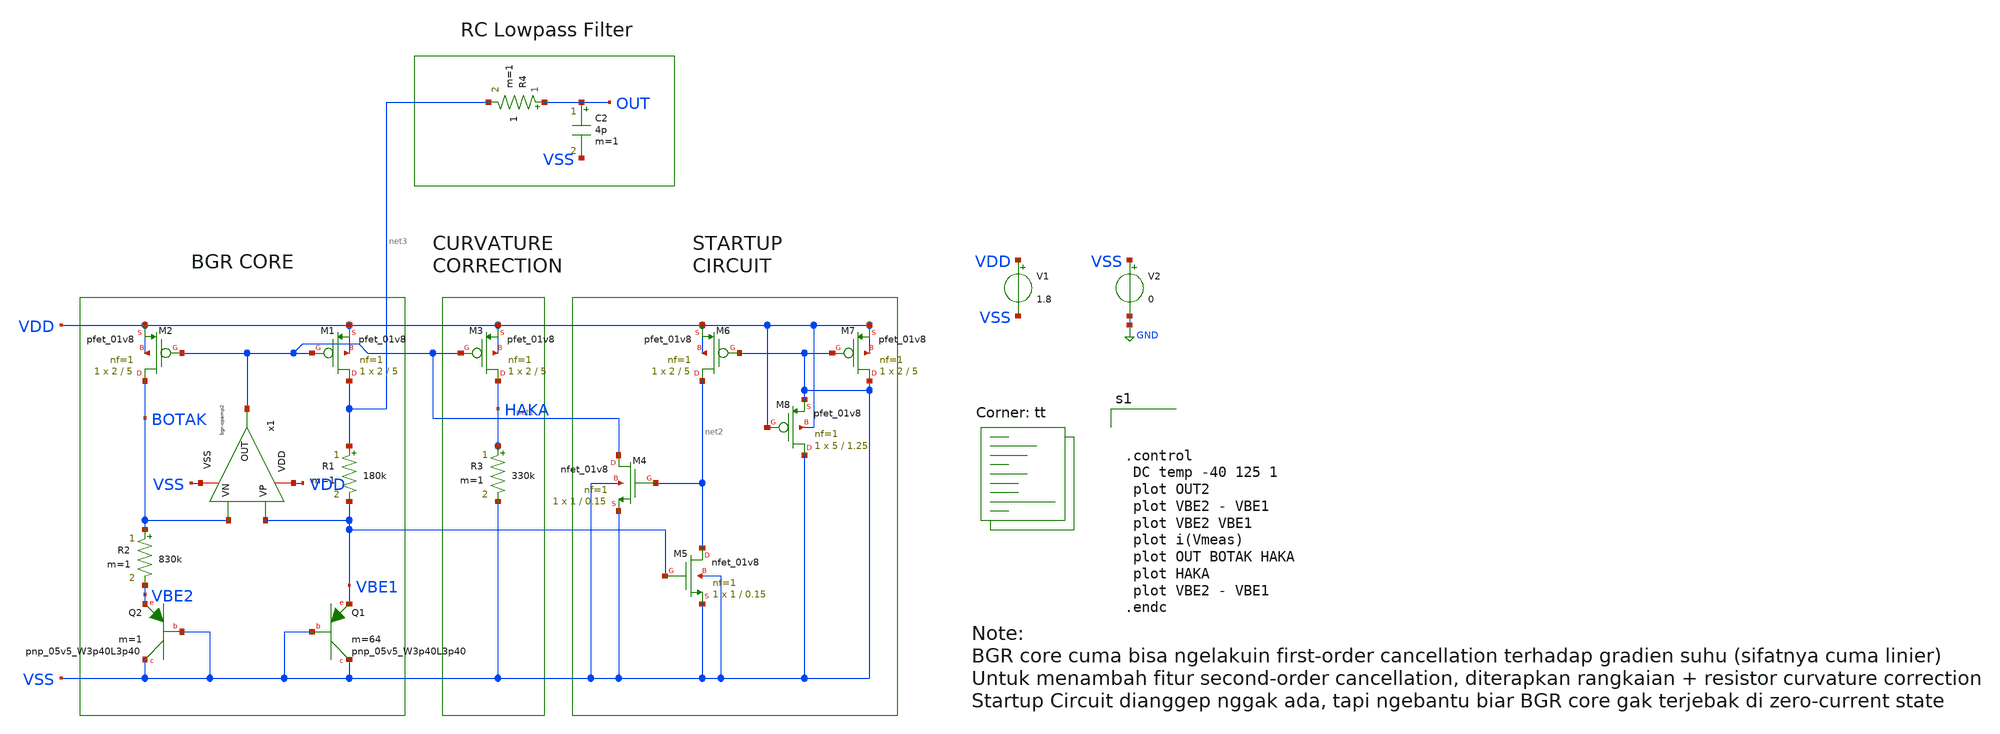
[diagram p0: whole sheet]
** sch_path: bandgap/bgr/bgr-core.sch
**.subckt bgr-core
XM1 net3 net1 VDD VDD sky130_fd_pr__pfet_01v8 L=5 W=2 nf=1 ad='int((nf+1)/2) * W/nf * 0.29' as='int((nf+2)/2) * W/nf * 0.29'
+ pd='2*int((nf+1)/2) * (W/nf + 0.29)' ps='2*int((nf+2)/2) * (W/nf + 0.29)' nrd='0.29 / W' nrs='0.29 / W'
+ sa=0 sb=0 sd=0 mult=1 m=1
XM2 BOTAK net1 VDD VDD sky130_fd_pr__pfet_01v8 L=5 W=2 nf=1 ad='int((nf+1)/2) * W/nf * 0.29' as='int((nf+2)/2) * W/nf * 0.29'
+ pd='2*int((nf+1)/2) * (W/nf + 0.29)' ps='2*int((nf+2)/2) * (W/nf + 0.29)' nrd='0.29 / W' nrs='0.29 / W'
+ sa=0 sb=0 sd=0 mult=1 m=1
R1 net3 VBE1 180k m=1
R2 BOTAK VBE2 830k m=1
XQ1 VSS VSS VBE1 sky130_fd_pr__pnp_05v5_W3p40L3p40 m=64
XQ2 VSS VSS VBE2 sky130_fd_pr__pnp_05v5_W3p40L3p40 m=1
V1 VDD VSS 1.8
V2 VSS GND 0
XM3 HAKA net1 VDD VDD sky130_fd_pr__pfet_01v8 L=5 W=2 nf=1 ad='int((nf+1)/2) * W/nf * 0.29' as='int((nf+2)/2) * W/nf * 0.29'
+ pd='2*int((nf+1)/2) * (W/nf + 0.29)' ps='2*int((nf+2)/2) * (W/nf + 0.29)' nrd='0.29 / W' nrs='0.29 / W'
+ sa=0 sb=0 sd=0 mult=1 m=1
R3 HAKA VSS 330k m=1
XM4 net1 net2 VSS VSS sky130_fd_pr__nfet_01v8 L=0.15 W=1 nf=1 ad='int((nf+1)/2) * W/nf * 0.29' as='int((nf+2)/2) * W/nf * 0.29'
+ pd='2*int((nf+1)/2) * (W/nf + 0.29)' ps='2*int((nf+2)/2) * (W/nf + 0.29)' nrd='0.29 / W' nrs='0.29 / W'
+ sa=0 sb=0 sd=0 mult=1 m=1
XM5 net2 VBE1 VSS VSS sky130_fd_pr__nfet_01v8 L=0.15 W=1 nf=1 ad='int((nf+1)/2) * W/nf * 0.29' as='int((nf+2)/2) * W/nf * 0.29'
+ pd='2*int((nf+1)/2) * (W/nf + 0.29)' ps='2*int((nf+2)/2) * (W/nf + 0.29)' nrd='0.29 / W' nrs='0.29 / W'
+ sa=0 sb=0 sd=0 mult=1 m=1
XM6 net2 VSS VDD VDD sky130_fd_pr__pfet_01v8 L=5 W=2 nf=1 ad='int((nf+1)/2) * W/nf * 0.29' as='int((nf+2)/2) * W/nf * 0.29'
+ pd='2*int((nf+1)/2) * (W/nf + 0.29)' ps='2*int((nf+2)/2) * (W/nf + 0.29)' nrd='0.29 / W' nrs='0.29 / W'
+ sa=0 sb=0 sd=0 mult=1 m=1
XM7 VSS VSS VDD VDD sky130_fd_pr__pfet_01v8 L=5 W=2 nf=1 ad='int((nf+1)/2) * W/nf * 0.29' as='int((nf+2)/2) * W/nf * 0.29'
+ pd='2*int((nf+1)/2) * (W/nf + 0.29)' ps='2*int((nf+2)/2) * (W/nf + 0.29)' nrd='0.29 / W' nrs='0.29 / W'
+ sa=0 sb=0 sd=0 mult=1 m=1
XM8 VSS VDD VSS VDD sky130_fd_pr__pfet_01v8 L=1.25 W=5 nf=1 ad='int((nf+1)/2) * W/nf * 0.29' as='int((nf+2)/2) * W/nf * 0.29'
+ pd='2*int((nf+1)/2) * (W/nf + 0.29)' ps='2*int((nf+2)/2) * (W/nf + 0.29)' nrd='0.29 / W' nrs='0.29 / W'
+ sa=0 sb=0 sd=0 mult=1 m=1
C2 OUT VSS 4p m=1
R4 OUT net3 1 m=1
x1 VDD net1 VBE1 BOTAK VSS bgr-opamp2
**** begin user architecture code
.lib $::SKYWATER_MODELS/sky130.lib.spice tt



.control
 DC temp -40 125 1
 plot OUT2
 plot VBE2 - VBE1
 plot VBE2 VBE1
 plot i(Vmeas)
 plot OUT BOTAK HAKA
 plot HAKA
 plot VBE2 - VBE1
.endc


**** end user architecture code
**.ends

* expanding   symbol:  afe-icdec-teknofest-2026/bandgap/bgr/bgr-opamp2.sym # of pins=5
** sym_path: bandgap/bgr/bgr-opamp2.sym
** sch_path: bandgap/bgr/bgr-opamp2.sch
.subckt bgr-opamp2 VDD OUT VP VN VSS
*.iopin VSS
*.iopin VDD
*.ipin VP
*.ipin VN
*.opin OUT
XR10 VSS net5 VSS sky130_fd_pr__res_high_po_1p41 L=9.235 mult=1 m=1
XM19 net2 net2 VSS VSS sky130_fd_pr__nfet_01v8_lvt L=0.5 W=6.4 nf=1 ad='int((nf+1)/2) * W/nf * 0.29'
+ as='int((nf+2)/2) * W/nf * 0.29' pd='2*int((nf+1)/2) * (W/nf + 0.29)' ps='2*int((nf+2)/2) * (W/nf + 0.29)'
+ nrd='0.29 / W' nrs='0.29 / W' sa=0 sb=0 sd=0 mult=1 m=1
XM20 net3 net2 net5 VSS sky130_fd_pr__nfet_01v8_lvt L=0.5 W=6.4 nf=1 ad='int((nf+1)/2) * W/nf * 0.29'
+ as='int((nf+2)/2) * W/nf * 0.29' pd='2*int((nf+1)/2) * (W/nf + 0.29)' ps='2*int((nf+2)/2) * (W/nf + 0.29)'
+ nrd='0.29 / W' nrs='0.29 / W' sa=0 sb=0 sd=0 mult=1 m=1
XM16 net4 net1 VDD VDD sky130_fd_pr__pfet_01v8_lvt L=0.5 W=20.8 nf=1 ad='int((nf+1)/2) * W/nf * 0.29'
+ as='int((nf+2)/2) * W/nf * 0.29' pd='2*int((nf+1)/2) * (W/nf + 0.29)' ps='2*int((nf+2)/2) * (W/nf + 0.29)'
+ nrd='0.29 / W' nrs='0.29 / W' sa=0 sb=0 sd=0 mult=1 m=1
XM13 net1 net1 VDD VDD sky130_fd_pr__pfet_01v8_lvt L=0.5 W=20.8 nf=1 ad='int((nf+1)/2) * W/nf * 0.29'
+ as='int((nf+2)/2) * W/nf * 0.29' pd='2*int((nf+1)/2) * (W/nf + 0.29)' ps='2*int((nf+2)/2) * (W/nf + 0.29)'
+ nrd='0.29 / W' nrs='0.29 / W' sa=0 sb=0 sd=0 mult=1 m=1
XM14 net2 net3 net4 VDD sky130_fd_pr__pfet_01v8_lvt L=0.5 W=20.8 nf=1 ad='int((nf+1)/2) * W/nf * 0.29'
+ as='int((nf+2)/2) * W/nf * 0.29' pd='2*int((nf+1)/2) * (W/nf + 0.29)' ps='2*int((nf+2)/2) * (W/nf + 0.29)'
+ nrd='0.29 / W' nrs='0.29 / W' sa=0 sb=0 sd=0 mult=1 m=1
XM17 net3 net3 net1 VDD sky130_fd_pr__pfet_01v8_lvt L=0.5 W=20.8 nf=1 ad='int((nf+1)/2) * W/nf * 0.29'
+ as='int((nf+2)/2) * W/nf * 0.29' pd='2*int((nf+1)/2) * (W/nf + 0.29)' ps='2*int((nf+2)/2) * (W/nf + 0.29)'
+ nrd='0.29 / W' nrs='0.29 / W' sa=0 sb=0 sd=0 mult=1 m=1
XM18 net6 net1 VDD VDD sky130_fd_pr__pfet_01v8_lvt L=0.5 W=20.8 nf=1 ad='int((nf+1)/2) * W/nf * 0.29'
+ as='int((nf+2)/2) * W/nf * 0.29' pd='2*int((nf+1)/2) * (W/nf + 0.29)' ps='2*int((nf+2)/2) * (W/nf + 0.29)'
+ nrd='0.29 / W' nrs='0.29 / W' sa=0 sb=0 sd=0 mult=1 m=1
XM21 net7 net3 net6 VDD sky130_fd_pr__pfet_01v8_lvt L=0.5 W=20.8 nf=1 ad='int((nf+1)/2) * W/nf * 0.29'
+ as='int((nf+2)/2) * W/nf * 0.29' pd='2*int((nf+1)/2) * (W/nf + 0.29)' ps='2*int((nf+2)/2) * (W/nf + 0.29)'
+ nrd='0.29 / W' nrs='0.29 / W' sa=0 sb=0 sd=0 mult=1 m=1
XM22 net7 net7 net9 VSS sky130_fd_pr__nfet_01v8_lvt L=0.5 W=1.45 nf=1 ad='int((nf+1)/2) * W/nf * 0.29'
+ as='int((nf+2)/2) * W/nf * 0.29' pd='2*int((nf+1)/2) * (W/nf + 0.29)' ps='2*int((nf+2)/2) * (W/nf + 0.29)'
+ nrd='0.29 / W' nrs='0.29 / W' sa=0 sb=0 sd=0 mult=1 m=1
XM23 net9 net7 net8 VSS sky130_fd_pr__nfet_01v8_lvt L=0.5 W=1.45 nf=1 ad='int((nf+1)/2) * W/nf * 0.29'
+ as='int((nf+2)/2) * W/nf * 0.29' pd='2*int((nf+1)/2) * (W/nf + 0.29)' ps='2*int((nf+2)/2) * (W/nf + 0.29)'
+ nrd='0.29 / W' nrs='0.29 / W' sa=0 sb=0 sd=0 mult=1 m=1
XM24 net8 net7 VSS VSS sky130_fd_pr__nfet_01v8_lvt L=0.5 W=1.45 nf=1 ad='int((nf+1)/2) * W/nf * 0.29'
+ as='int((nf+2)/2) * W/nf * 0.29' pd='2*int((nf+1)/2) * (W/nf + 0.29)' ps='2*int((nf+2)/2) * (W/nf + 0.29)'
+ nrd='0.29 / W' nrs='0.29 / W' sa=0 sb=0 sd=0 mult=1 m=1
XM26 net15 VN net10 VDD sky130_fd_pr__pfet_01v8_lvt L=1.25 W=30 nf=1 ad='int((nf+1)/2) * W/nf * 0.29'
+ as='int((nf+2)/2) * W/nf * 0.29' pd='2*int((nf+1)/2) * (W/nf + 0.29)' ps='2*int((nf+2)/2) * (W/nf + 0.29)'
+ nrd='0.29 / W' nrs='0.29 / W' sa=0 sb=0 sd=0 mult=1 m=1
XM27 net14 VP net10 VDD sky130_fd_pr__pfet_01v8_lvt L=1.25 W=30 nf=1 ad='int((nf+1)/2) * W/nf * 0.29'
+ as='int((nf+2)/2) * W/nf * 0.29' pd='2*int((nf+1)/2) * (W/nf + 0.29)' ps='2*int((nf+2)/2) * (W/nf + 0.29)'
+ nrd='0.29 / W' nrs='0.29 / W' sa=0 sb=0 sd=0 mult=1 m=1
XM15 net10 net1 VDD VDD sky130_fd_pr__pfet_01v8_lvt L=1.25 W=20.8 nf=1 ad='int((nf+1)/2) * W/nf * 0.29'
+ as='int((nf+2)/2) * W/nf * 0.29' pd='2*int((nf+1)/2) * (W/nf + 0.29)' ps='2*int((nf+2)/2) * (W/nf + 0.29)'
+ nrd='0.29 / W' nrs='0.29 / W' sa=0 sb=0 sd=0 mult=1 m=1
XM25 net12 net1 VDD VDD sky130_fd_pr__pfet_01v8_lvt L=1.25 W=10.4 nf=1 ad='int((nf+1)/2) * W/nf * 0.29'
+ as='int((nf+2)/2) * W/nf * 0.29' pd='2*int((nf+1)/2) * (W/nf + 0.29)' ps='2*int((nf+2)/2) * (W/nf + 0.29)'
+ nrd='0.29 / W' nrs='0.29 / W' sa=0 sb=0 sd=0 mult=1 m=1
XM28 net13 net1 VDD VDD sky130_fd_pr__pfet_01v8_lvt L=1.25 W=10.4 nf=1 ad='int((nf+1)/2) * W/nf * 0.29'
+ as='int((nf+2)/2) * W/nf * 0.29' pd='2*int((nf+1)/2) * (W/nf + 0.29)' ps='2*int((nf+2)/2) * (W/nf + 0.29)'
+ nrd='0.29 / W' nrs='0.29 / W' sa=0 sb=0 sd=0 mult=1 m=1
XM29 OUT net3 net12 VDD sky130_fd_pr__pfet_01v8_lvt L=1.25 W=10.4 nf=1 ad='int((nf+1)/2) * W/nf * 0.29'
+ as='int((nf+2)/2) * W/nf * 0.29' pd='2*int((nf+1)/2) * (W/nf + 0.29)' ps='2*int((nf+2)/2) * (W/nf + 0.29)'
+ nrd='0.29 / W' nrs='0.29 / W' sa=0 sb=0 sd=0 mult=1 m=1
XM30 net11 net3 net13 VDD sky130_fd_pr__pfet_01v8_lvt L=1.25 W=10.4 nf=1 ad='int((nf+1)/2) * W/nf * 0.29'
+ as='int((nf+2)/2) * W/nf * 0.29' pd='2*int((nf+1)/2) * (W/nf + 0.29)' ps='2*int((nf+2)/2) * (W/nf + 0.29)'
+ nrd='0.29 / W' nrs='0.29 / W' sa=0 sb=0 sd=0 mult=1 m=1
XM31 OUT net7 net15 VSS sky130_fd_pr__nfet_01v8_lvt L=1.25 W=2.4 nf=1 ad='int((nf+1)/2) * W/nf * 0.29'
+ as='int((nf+2)/2) * W/nf * 0.29' pd='2*int((nf+1)/2) * (W/nf + 0.29)' ps='2*int((nf+2)/2) * (W/nf + 0.29)'
+ nrd='0.29 / W' nrs='0.29 / W' sa=0 sb=0 sd=0 mult=1 m=1
XM32 net11 net7 net14 VSS sky130_fd_pr__nfet_01v8_lvt L=1.25 W=2.4 nf=1 ad='int((nf+1)/2) * W/nf * 0.29'
+ as='int((nf+2)/2) * W/nf * 0.29' pd='2*int((nf+1)/2) * (W/nf + 0.29)' ps='2*int((nf+2)/2) * (W/nf + 0.29)'
+ nrd='0.29 / W' nrs='0.29 / W' sa=0 sb=0 sd=0 mult=1 m=1
XM33 net15 net11 VSS VSS sky130_fd_pr__nfet_01v8_lvt L=1.25 W=2.4 nf=1 ad='int((nf+1)/2) * W/nf * 0.29'
+ as='int((nf+2)/2) * W/nf * 0.29' pd='2*int((nf+1)/2) * (W/nf + 0.29)' ps='2*int((nf+2)/2) * (W/nf + 0.29)'
+ nrd='0.29 / W' nrs='0.29 / W' sa=0 sb=0 sd=0 mult=1 m=1
XM34 net14 net11 VSS VSS sky130_fd_pr__nfet_01v8_lvt L=1.25 W=2.4 nf=1 ad='int((nf+1)/2) * W/nf * 0.29'
+ as='int((nf+2)/2) * W/nf * 0.29' pd='2*int((nf+1)/2) * (W/nf + 0.29)' ps='2*int((nf+2)/2) * (W/nf + 0.29)'
+ nrd='0.29 / W' nrs='0.29 / W' sa=0 sb=0 sd=0 mult=1 m=1
.ends

.GLOBAL GND
.end
